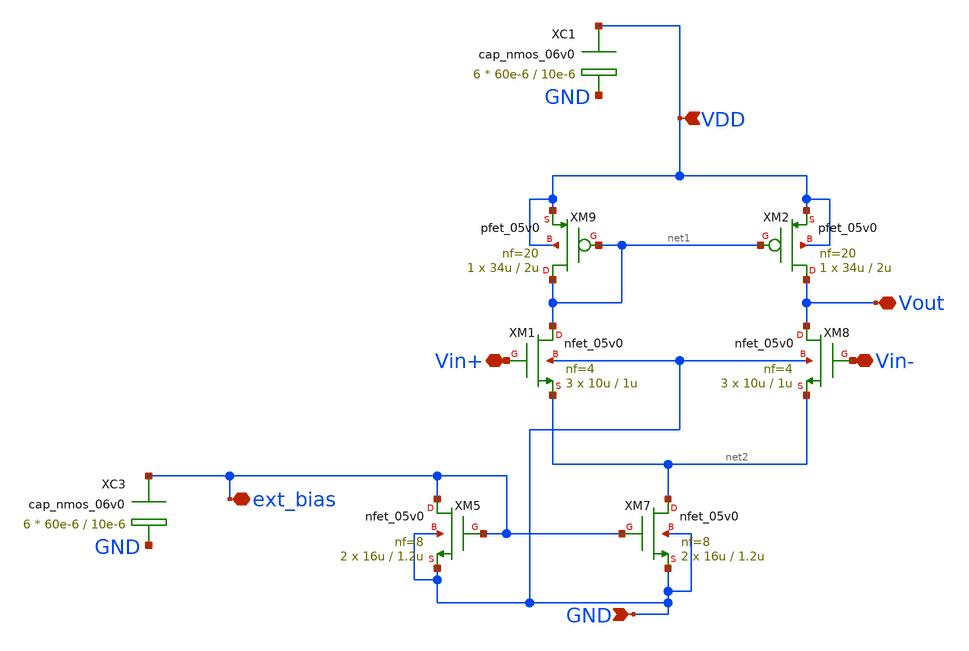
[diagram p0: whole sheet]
** sch_path: TG_gm_ff_testing/gm_ff.sch
**.subckt gm_ff GND ext_bias Vin- Vin+ Vout VDD
*.ipin GND
*.iopin ext_bias
*.iopin Vin-
*.iopin Vin+
*.iopin Vout
*.ipin VDD
XC3 ext_bias GND cap_nmos_06v0 c_width=60e-6 c_length=10e-6 m=6
XC1 VDD GND cap_nmos_06v0 c_width=60e-6 c_length=10e-6 m=6
XM7 net2 ext_bias GND GND nfet_05v0 L=1.2u W=16u nf=8 ad='int((nf+1)/2) * W/nf * 0.18u' as='int((nf+2)/2) * W/nf * 0.18u'
+ pd='2*int((nf+1)/2) * (W/nf + 0.18u)' ps='2*int((nf+2)/2) * (W/nf + 0.18u)' nrd='0.18u / W' nrs='0.18u / W'
+ sa=0 sb=0 sd=0 m=2
XM8 Vout Vin- net2 GND nfet_05v0 L=1u W=10u nf=4 ad='int((nf+1)/2) * W/nf * 0.18u' as='int((nf+2)/2) * W/nf * 0.18u'
+ pd='2*int((nf+1)/2) * (W/nf + 0.18u)' ps='2*int((nf+2)/2) * (W/nf + 0.18u)' nrd='0.18u / W' nrs='0.18u / W'
+ sa=0 sb=0 sd=0 m=3
XM9 net1 net1 VDD VDD pfet_05v0 L=2u W=34u nf=20 ad='int((nf+1)/2) * W/nf * 0.18u' as='int((nf+2)/2) * W/nf * 0.18u'
+ pd='2*int((nf+1)/2) * (W/nf + 0.18u)' ps='2*int((nf+2)/2) * (W/nf + 0.18u)' nrd='0.18u / W' nrs='0.18u / W'
+ sa=0 sb=0 sd=0 m=1
XM5 ext_bias ext_bias GND GND nfet_05v0 L=1.2u W=16u nf=8 ad='int((nf+1)/2) * W/nf * 0.18u' as='int((nf+2)/2) * W/nf * 0.18u'
+ pd='2*int((nf+1)/2) * (W/nf + 0.18u)' ps='2*int((nf+2)/2) * (W/nf + 0.18u)' nrd='0.18u / W' nrs='0.18u / W'
+ sa=0 sb=0 sd=0 m=2
XM1 net1 Vin+ net2 GND nfet_05v0 L=1u W=10u nf=4 ad='int((nf+1)/2) * W/nf * 0.18u' as='int((nf+2)/2) * W/nf * 0.18u'
+ pd='2*int((nf+1)/2) * (W/nf + 0.18u)' ps='2*int((nf+2)/2) * (W/nf + 0.18u)' nrd='0.18u / W' nrs='0.18u / W'
+ sa=0 sb=0 sd=0 m=3
XM2 Vout net1 VDD VDD pfet_05v0 L=2u W=34u nf=20 ad='int((nf+1)/2) * W/nf * 0.18u' as='int((nf+2)/2) * W/nf * 0.18u'
+ pd='2*int((nf+1)/2) * (W/nf + 0.18u)' ps='2*int((nf+2)/2) * (W/nf + 0.18u)' nrd='0.18u / W' nrs='0.18u / W'
+ sa=0 sb=0 sd=0 m=1
**.ends
.end
